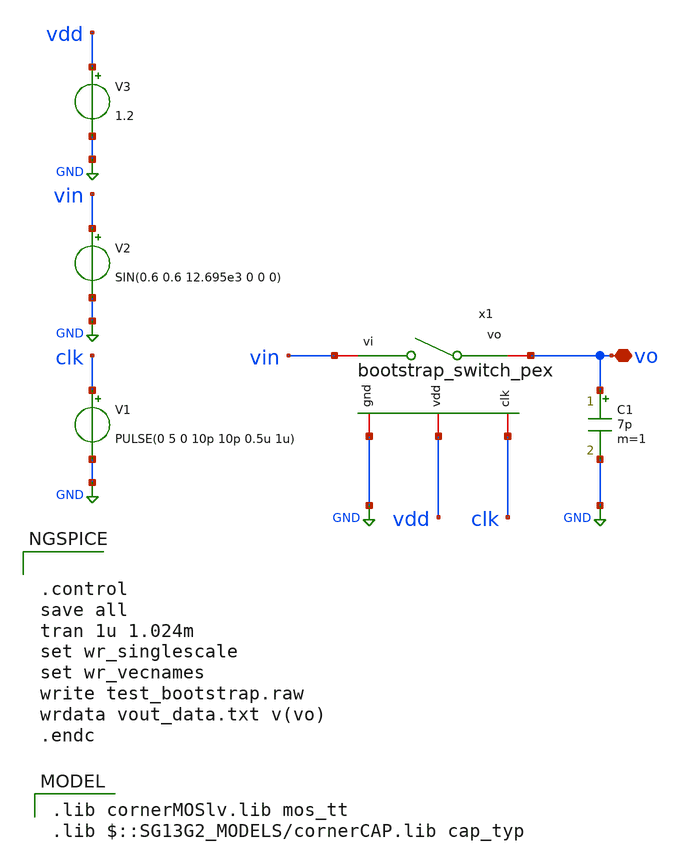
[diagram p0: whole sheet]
** sch_path: dependencies/ADC/ADC-main/schematic/xschem/boostrap_switch_tb_ps.sch
**.subckt boostrap_switch_tb_ps vo
*.iopin vo
V1 clk GND PULSE(0 5 0 10p 10p 0.5u 1u)
V2 vin GND SIN(0.6 0.6 12.695e3 0 0 0)
V3 vdd GND 1.2
C1 vo GND 7p m=1
x1 vdd vin vo clk GND bootstrap_switch_pex
**** begin user architecture code
 .lib cornerMOSlv.lib mos_tt
.lib $::SG13G2_MODELS/cornerCAP.lib cap_typ



.control
save all
tran 1u 1.024m
set wr_singlescale
set wr_vecnames
write test_bootstrap.raw
wrdata vout_data.txt v(vo)
.endc


**** end user architecture code
**.ends

* expanding   symbol:  /home/tien/SAR_ADC_8BIT_IHP/xschem/xschem_pex_symbol/bootstrap_switch_pex.sym
*+ # of pins=5
** sym_path: dependencies/ADC/ADC-main/netlist/pex/xschem_pex_symbol/bootstrap_switch.sym

.subckt bootstrap_switch_pex vdd vi vo clk gnd
X0 gnd.t12 a_1896_n484# a_1378_n288.t0 gnd.t11 sg13_lv_nmos ad=0.136p pd=1.48u as=0.136p ps=1.48u
+ w=0.4u l=0.13u
X1 vi.t0 a_777_n1200.t2 vo.t0 gnd.t4 sg13_lv_nmos ad=0.85p pd=5.68u as=0.85p ps=5.68u w=2.5u l=0.13u
X2 gnd.t15 a_1594_n1108.t3 a_2897_n1624.t0 gnd.t14 sg13_lv_nmos ad=0.136p pd=1.48u as=0.136p
+ ps=1.48u w=0.4u l=0.13u
X3 a_1044_n1116.t0 a_1896_n484# vdd.t6 vdd.t4 sg13_lv_pmos ad=0.17p pd=1.68u as=0.17p ps=1.68u
+ w=0.5u l=0.13u
X4 vdd.t3 clk.t0 a_1594_n1108.t2 vdd.t1 sg13_lv_pmos ad=0.272p pd=2.28u as=0.272p ps=2.28u w=0.8u
+ l=0.13u
X5 vdd.t8 a_2905_n460.t1 w_1241_n212.t2 gnd.t17 sg13_lv_nmos ad=0.442p pd=3.28u as=0.442p ps=3.28u
+ w=1.3u l=0.13u
X6 w_1241_n212.t3 a_1107_n1758.t0 cap_cmim l=6.99u w=9.39u
X7 a_2217_n1270.t0 a_1594_n1108.t4 gnd.t3 gnd.t2 sg13_lv_nmos ad=0.17p pd=1.68u as=0.17p ps=1.68u
+ w=0.5u l=0.13u
X8 a_777_n1200.t0 vdd.t9 a_2217_n1270.t1 gnd.t6 sg13_lv_nmos ad=0.17p pd=1.68u as=0.17p ps=1.68u
+ w=0.5u l=0.13u
X9 gnd.t8 clk.t0 a_1594_n1108.t1 gnd.t7 sg13_lv_nmos ad=0.136p pd=1.48u as=0.136p ps=1.48u w=0.4u
+ l=0.13u
X10 vdd.t5 a_1896_n484# a_1378_n288.t1 vdd.t4 sg13_lv_pmos ad=0.272p pd=2.28u as=0.272p ps=2.28u
+ w=0.8u l=0.13u
X11 vdd.t2 a_1594_n1108.t3 a_2897_n1624.t1 vdd.t1 sg13_lv_pmos ad=0.272p pd=2.28u as=0.272p ps=2.28u
+ w=0.8u l=0.13u
X12 a_2905_n460.t2 a_1594_n1108.t0 cap_cmim l=6.99u w=4.665u
X13 gnd.t1 a_1594_n1108.t5 a_1426_n1756.t0 gnd.t0 sg13_lv_nmos ad=1.02p pd=6.68u as=1.02p ps=6.68u
+ w=3u l=0.13u
X14 a_1107_n1758.t2 a_1044_n1116.t2 vi.t1 gnd.t16 sg13_lv_nmos ad=1.02p pd=6.68u as=1.02p ps=6.68u
+ w=3u l=0.13u
X15 a_3245_n350.t1 a_2897_n1624.t2 cap_cmim l=6.99u w=4.665u
X16 w_1241_n212.t1 a_1378_n288.t2 a_777_n1200.t1 w_1241_n212.t0 sg13_lv_pmos ad=0.17p pd=1.68u
+ as=0.17p ps=1.68u w=0.5u l=0.13u
X17 a_1107_n1758.t1 a_1594_n1108.t6 gnd.t10 gnd.t9 sg13_lv_nmos ad=0.442p pd=3.28u as=0.442p
+ ps=3.28u w=1.3u l=0.4u
X18 a_3245_n350.t0 a_2905_n460.t3 vdd.t0 gnd.t5 sg13_lv_nmos ad=0.442p pd=3.28u as=0.442p ps=3.28u
+ w=1.3u l=0.13u
X19 vdd.t7 a_3245_n350.t2 a_2905_n460.t0 gnd.t13 sg13_lv_nmos ad=0.442p pd=3.28u as=0.442p ps=3.28u
+ w=1.3u l=0.13u
X20 a_1426_n1756.t1 vdd.t10 a_1044_n1116.t1 gnd.t0 sg13_lv_nmos ad=1.02p pd=6.68u as=1.02p ps=6.68u
+ w=3u l=0.13u
C0 a_1896_n484# vdd 0.22188f
C1 vdd vi 0.08373f
C2 vdd clk 0.16174f
C3 vo vi 0.61887f
C4 vo vdd 0.04889f
R0 a_1378_n288.t0 a_1378_n288.n0 17.2852
R1 a_1378_n288.n0 a_1378_n288.t2 16.1733
R2 a_1378_n288.n0 a_1378_n288.t1 9.11151
R3 gnd.n47 gnd.t11 6064.32
R4 gnd.t6 gnd.n18 5073.33
R5 gnd.n58 gnd.n57 4035.37
R6 gnd.n46 gnd.n45 2743.13
R7 gnd.n47 gnd.n46 2249.79
R8 gnd.n45 gnd.t6 1906.67
R9 gnd.n58 gnd.n18 1486.67
R10 gnd.n52 gnd.n51 1186.91
R11 gnd.n55 gnd.n54 447.637
R12 gnd.n63 gnd.n62 302.812
R13 gnd.n59 gnd.n58 181.311
R14 gnd.n63 gnd.t11 123.954
R15 gnd.n52 gnd.t7 82.2655
R16 gnd.n55 gnd.t14 82.2655
R17 gnd.n48 gnd.n47 68.6012
R18 gnd.t17 gnd.n48 65.5295
R19 gnd.n50 gnd.t5 64.9886
R20 gnd.t9 gnd.n59 57.7882
R21 gnd.t13 gnd.n50 49.6349
R22 gnd.t2 gnd.n61 49.0963
R23 gnd.n62 gnd.t2 47.2961
R24 gnd.t16 gnd.t4 40.5082
R25 gnd.n61 gnd.t0 38.6369
R26 gnd.n51 gnd.t13 35.3194
R27 gnd.n60 gnd.t9 31.9293
R28 gnd.n5 gnd.t3 30.9467
R29 gnd.t5 gnd.n49 20.985
R30 gnd.n22 gnd.t8 17.4482
R31 gnd.n64 gnd.t12 17.3778
R32 gnd.n20 gnd.t15 17.3608
R33 gnd.n53 gnd.n52 17.0005
R34 gnd.n56 gnd.n21 17.0005
R35 gnd.n56 gnd.n55 17.0005
R36 gnd.n33 gnd.n19 12.7958
R37 gnd.t4 gnd.n60 12.4856
R38 gnd.n49 gnd.t17 11.7634
R39 gnd.n54 gnd.t7 11.7395
R40 gnd.n57 gnd.t14 11.7395
R41 gnd.n64 gnd.n63 11.3338
R42 gnd.n8 gnd.n7 9.03042
R43 gnd.n74 gnd.n73 9.03042
R44 gnd.n36 gnd.n35 9.03042
R45 gnd.n40 gnd.n39 9.03042
R46 gnd.n72 gnd.n71 9.01861
R47 gnd.n7 gnd.n6 9.0186
R48 gnd.n35 gnd.n34 9.0186
R49 gnd.n27 gnd.n23 9.01787
R50 gnd.n4 gnd.n1 9.01787
R51 gnd.n68 gnd.n10 9.01787
R52 gnd.n32 gnd.n29 9.01787
R53 gnd.n28 gnd.n27 9.01787
R54 gnd.n5 gnd.n4 9.0005
R55 gnd.n3 gnd.n2 9.0005
R56 gnd.n12 gnd.n11 9.0005
R57 gnd.n73 gnd.n72 9.0005
R58 gnd.n13 gnd.n12 9.0005
R59 gnd.n69 gnd.n68 9.0005
R60 gnd.n70 gnd.n69 9.0005
R61 gnd.n31 gnd.n30 9.0005
R62 gnd.n33 gnd.n32 9.0005
R63 gnd.n43 gnd.n42 9.0005
R64 gnd.n25 gnd.n24 9.0005
R65 gnd.n42 gnd.n41 9.0005
R66 gnd.n26 gnd.n25 9.0005
R67 gnd.n41 gnd.n40 9.0005
R68 gnd.n56 gnd.n19 8.52716
R69 gnd.n45 gnd.n17 8.501
R70 gnd.n18 gnd.n16 8.5005
R71 gnd.n48 gnd.n44 8.5005
R72 gnd.n14 gnd.t10 5.65073
R73 gnd.n53 gnd.n22 5.63152
R74 gnd.n43 gnd.n23 4.5471
R75 gnd.n71 gnd.n70 4.54536
R76 gnd.n6 gnd.n5 4.53473
R77 gnd.n34 gnd.n33 4.53473
R78 gnd.n8 gnd.n1 4.50628
R79 gnd.n74 gnd.n10 4.50628
R80 gnd.n36 gnd.n29 4.50628
R81 gnd.n39 gnd.n28 4.50628
R82 gnd.n9 gnd.n8 3.3005
R83 gnd.n39 gnd.n38 3.3005
R84 gnd.n37 gnd.n36 3.3005
R85 gnd.n75 gnd.n74 3.3005
R86 gnd.n44 gnd.n43 2.86049
R87 gnd.n60 gnd.n16 2.66376
R88 gnd.n65 gnd.n17 2.64957
R89 gnd.n57 gnd.n56 2.63175
R90 gnd.n54 gnd.n53 2.63175
R91 gnd.n14 gnd.t1 2.28269
R92 gnd.n70 gnd.n67 2.02138
R93 gnd.t0 gnd.t16 1.62081
R94 gnd.n67 gnd.n66 1.15699
R95 gnd.n67 gnd.n15 0.961754
R96 gnd.n66 gnd.n65 0.859819
R97 gnd.n15 gnd.n14 0.745431
R98 gnd.n22 gnd.n21 0.712801
R99 gnd.n38 gnd.n37 0.52124
R100 gnd.n61 gnd.n16 0.515338
R101 gnd.n16 gnd.n15 0.431601
R102 gnd gnd.n0 0.270611
R103 gnd.n66 gnd.n16 0.199062
R104 gnd.n65 gnd.n64 0.176594
R105 gnd gnd.n76 0.168643
R106 gnd.n76 gnd.n75 0.108906
R107 gnd.n38 gnd.n0 0.0950175
R108 gnd.n20 gnd.n19 0.0773493
R109 gnd gnd.n0 0.0583436
R110 gnd.n75 gnd.n9 0.045325
R111 gnd.n21 gnd.n20 0.0396781
R112 gnd.n7 gnd.n2 0.0357
R113 gnd.n73 gnd.n11 0.0357
R114 gnd.n72 gnd.n12 0.0357
R115 gnd.n35 gnd.n30 0.0357
R116 gnd.n42 gnd.n24 0.0357
R117 gnd.n41 gnd.n25 0.0357
R118 gnd.n40 gnd.n26 0.0357
R119 gnd.n4 gnd.n3 0.0342333
R120 gnd.n68 gnd.n12 0.0342333
R121 gnd.n69 gnd.n13 0.0342333
R122 gnd.n32 gnd.n31 0.0342333
R123 gnd.n27 gnd.n25 0.0342333
R124 gnd.n76 gnd 0.0319332
R125 gnd.n37 gnd.n9 0.0237925
R126 gnd.n6 gnd.n3 0.0185314
R127 gnd.n34 gnd.n31 0.0185314
R128 gnd.n71 gnd.n13 0.0185229
R129 gnd.n2 gnd.n1 0.0178037
R130 gnd.n11 gnd.n10 0.0178037
R131 gnd.n30 gnd.n29 0.0178037
R132 gnd.n28 gnd.n26 0.0178037
R133 gnd.n24 gnd.n23 0.0177958
R134 gnd.n50 gnd.n44 0.00944882
R135 gnd.n62 gnd.n16 0.00513002
R136 gnd.n59 gnd.n16 0.00247443
R137 gnd.n49 gnd.n44 0.00215079
R138 gnd.n51 gnd.n44 0.00129651
R139 gnd.n17 gnd.n16 0.00124999
R140 gnd.n46 gnd.n44 0.00100002
R141 a_777_n1200.t0 a_777_n1200.n0 30.6412
R142 a_777_n1200.n0 a_777_n1200.t1 28.4911
R143 a_777_n1200.n0 a_777_n1200.t2 24.8453
R144 vo vo.t0 8.55687
R145 vi vi.n2 8.03514
R146 vi.n1 vi.t0 5.67075
R147 vi.n1 vi.t1 5.66684
R148 vi.t0 vi.n0 4.24477
R149 vi.t1 vi.n0 3.42449
R150 vi.n2 vi.n1 0.059708
R151 vi.n2 vi.n0 0.042166
R152 a_1594_n1108.n11 a_1594_n1108.n10 32.6771
R153 a_1594_n1108.n7 a_1594_n1108.t1 17.2852
R154 a_1594_n1108.n9 a_1594_n1108.t4 15.8888
R155 a_1594_n1108.n9 a_1594_n1108.t6 15.8447
R156 a_1594_n1108.n8 a_1594_n1108.t3 15.4458
R157 a_1594_n1108.n10 a_1594_n1108.t5 15.0018
R158 a_1594_n1108.n19 a_1594_n1108.n11 10.3793
R159 a_1594_n1108.n11 a_1594_n1108.n8 10.3449
R160 a_1594_n1108.n7 a_1594_n1108.t2 9.11151
R161 a_1594_n1108.n18 a_1594_n1108.n12 9.0005
R162 a_1594_n1108.n19 a_1594_n1108.n18 9.0005
R163 a_1594_n1108.n4 a_1594_n1108.n3 9.0005
R164 a_1594_n1108.n22 a_1594_n1108.n21 9.0005
R165 a_1594_n1108.n14 a_1594_n1108.n6 4.52049
R166 a_1594_n1108.n13 a_1594_n1108.n5 4.51458
R167 a_1594_n1108.n23 a_1594_n1108.n1 4.50536
R168 a_1594_n1108.n14 a_1594_n1108.n2 4.5005
R169 a_1594_n1108.n25 a_1594_n1108.n24 4.5005
R170 a_1594_n1108.n17 a_1594_n1108.n1 4.49517
R171 a_1594_n1108.n26 a_1594_n1108.n0 4.49343
R172 a_1594_n1108.n16 a_1594_n1108.n15 4.49343
R173 a_1594_n1108.n20 a_1594_n1108.n19 4.4932
R174 a_1594_n1108.n15 a_1594_n1108.n13 4.49154
R175 a_1594_n1108.n19 a_1594_n1108.n6 4.49125
R176 a_1594_n1108.n18 a_1594_n1108.n17 3.0005
R177 a_1594_n1108.n24 a_1594_n1108.n2 3.0005
R178 a_1594_n1108.t0 a_1594_n1108.n27 0.777833
R179 a_1594_n1108.n10 a_1594_n1108.n9 0.59856
R180 a_1594_n1108.n8 a_1594_n1108.n7 0.570828
R181 a_1594_n1108.n27 a_1594_n1108.n26 0.106207
R182 a_1594_n1108.n13 a_1594_n1108.n6 0.0402971
R183 a_1594_n1108.n25 a_1594_n1108.n1 0.0239239
R184 a_1594_n1108.n20 a_1594_n1108.n2 0.0166005
R185 a_1594_n1108.n21 a_1594_n1108.n20 0.0166005
R186 a_1594_n1108.n23 a_1594_n1108.n22 0.0166005
R187 a_1594_n1108.n24 a_1594_n1108.n23 0.0166005
R188 a_1594_n1108.n3 a_1594_n1108.n0 0.0161469
R189 a_1594_n1108.n17 a_1594_n1108.n0 0.0161469
R190 a_1594_n1108.n16 a_1594_n1108.n4 0.0161469
R191 a_1594_n1108.n18 a_1594_n1108.n16 0.0161469
R192 a_1594_n1108.t0 a_1594_n1108.n27 0.0129943
R193 a_1594_n1108.n12 a_1594_n1108.n5 0.0126912
R194 a_1594_n1108.n19 a_1594_n1108.n5 0.0126912
R195 a_1594_n1108.n14 a_1594_n1108.n12 0.0118028
R196 a_1594_n1108.n15 a_1594_n1108.n14 0.0115336
R197 a_1594_n1108.n26 a_1594_n1108.n25 0.0115
R198 a_1594_n1108.n21 a_1594_n1108.n4 0.000803448
R199 a_1594_n1108.n22 a_1594_n1108.n3 0.000803448
R200 a_2897_n1624.n22 a_2897_n1624.n21 31.0822
R201 a_2897_n1624.t0 a_2897_n1624.n22 17.2852
R202 a_2897_n1624.n22 a_2897_n1624.t1 9.11151
R203 a_2897_n1624.n11 a_2897_n1624.n8 9.0005
R204 a_2897_n1624.n5 a_2897_n1624.n3 9.0005
R205 a_2897_n1624.n11 a_2897_n1624.n10 9.0005
R206 a_2897_n1624.n9 a_2897_n1624.n3 9.0005
R207 a_2897_n1624.n19 a_2897_n1624.n2 4.50722
R208 a_2897_n1624.n15 a_2897_n1624.n14 4.50536
R209 a_2897_n1624.n16 a_2897_n1624.n4 4.5005
R210 a_2897_n1624.n19 a_2897_n1624.n18 4.5005
R211 a_2897_n1624.n14 a_2897_n1624.n13 4.49517
R212 a_2897_n1624.n20 a_2897_n1624.n1 4.4937
R213 a_2897_n1624.n7 a_2897_n1624.n6 4.49343
R214 a_2897_n1624.n21 a_2897_n1624.n0 4.4932
R215 a_2897_n1624.n13 a_2897_n1624.n12 3.0005
R216 a_2897_n1624.n17 a_2897_n1624.n16 3.0005
R217 a_2897_n1624.n12 a_2897_n1624.n1 3.0005
R218 a_2897_n1624.n18 a_2897_n1624.n17 3.0005
R219 a_2897_n1624.n6 a_2897_n1624.t2 0.119227
R220 a_2897_n1624.n17 a_2897_n1624.n3 0.0317552
R221 a_2897_n1624.n12 a_2897_n1624.n11 0.0308448
R222 a_2897_n1624.n20 a_2897_n1624.n19 0.0297377
R223 a_2897_n1624.n14 a_2897_n1624.n4 0.0239239
R224 a_2897_n1624.n15 a_2897_n1624.n5 0.0166005
R225 a_2897_n1624.n16 a_2897_n1624.n15 0.0166005
R226 a_2897_n1624.n18 a_2897_n1624.n0 0.0166005
R227 a_2897_n1624.n9 a_2897_n1624.n0 0.0166005
R228 a_2897_n1624.n10 a_2897_n1624.n2 0.0161469
R229 a_2897_n1624.n2 a_2897_n1624.n1 0.0161469
R230 a_2897_n1624.n8 a_2897_n1624.n7 0.0161469
R231 a_2897_n1624.n13 a_2897_n1624.n7 0.0161469
R232 a_2897_n1624.n21 a_2897_n1624.n20 0.0156093
R233 a_2897_n1624.n6 a_2897_n1624.n4 0.0115
R234 a_2897_n1624.n8 a_2897_n1624.n5 0.000803448
R235 a_2897_n1624.n11 a_2897_n1624.n3 0.000803448
R236 a_2897_n1624.n10 a_2897_n1624.n9 0.000803448
R237 vdd.n22 vdd.t10 37.129
R238 vdd.n21 vdd.t7 21.2951
R239 vdd.n6 vdd.t6 17.5186
R240 vdd.n2 vdd.n0 17.0005
R241 vdd.t0 vdd.n15 17.0005
R242 vdd.n17 vdd.t0 17.0005
R243 vdd.n16 vdd.t0 17.0005
R244 vdd.t8 vdd.n15 17.0005
R245 vdd.n17 vdd.t8 17.0005
R246 vdd.t8 vdd.n16 17.0005
R247 vdd.n5 vdd.t9 15.4454
R248 vdd.n13 vdd.n12 15.1399
R249 vdd.n20 vdd.n19 12.5536
R250 vdd.n1 vdd.t1 11.2968
R251 vdd.n1 vdd.t3 9.01184
R252 vdd.n19 vdd.n18 9.0005
R253 vdd.n3 vdd.t2 8.91901
R254 vdd.n9 vdd.t5 8.91901
R255 vdd.n10 vdd.n9 8.60851
R256 vdd.n12 vdd.n11 8.501
R257 vdd.n4 vdd.n0 8.46974
R258 vdd.n8 vdd.n7 8.46936
R259 vdd.n11 vdd.t4 5.66842
R260 vdd.t4 vdd.n10 5.66778
R261 vdd.t1 vdd.n0 5.66717
R262 vdd.n19 vdd.n14 4.648
R263 vdd.n6 vdd.n5 3.95314
R264 vdd.n22 vdd.n21 0.908402
R265 vdd.n2 vdd.n1 0.717193
R266 vdd.n5 vdd.n4 0.370276
R267 vdd vdd.n22 0.23247
R268 vdd vdd.n13 0.168921
R269 vdd.n8 vdd.n6 0.164989
R270 vdd.n4 vdd.n3 0.139431
R271 vdd.n9 vdd.n8 0.116961
R272 vdd.n3 vdd.n2 0.0531761
R273 vdd.n20 vdd.n13 0.0498354
R274 vdd.n18 vdd.n17 0.0452964
R275 vdd.n21 vdd.n20 0.0287622
R276 vdd.n16 vdd.n14 0.0274732
R277 vdd.n17 vdd.n14 0.024195
R278 vdd.n18 vdd.n15 0.00547738
R279 vdd.n12 vdd.n6 0.00173596
R280 vdd.n10 vdd.n7 0.00166667
R281 vdd.n11 vdd.n7 0.00124999
R282 a_1044_n1116.t0 a_1044_n1116.n0 57.304
R283 a_1044_n1116.n0 a_1044_n1116.t2 15.0005
R284 a_1044_n1116.n0 a_1044_n1116.t1 3.77826
R285 clk clk.t0 39.2421
R286 a_2905_n460.n20 a_2905_n460.n19 21.2719
R287 a_2905_n460.n20 a_2905_n460.t1 15.858
R288 a_2905_n460.n21 a_2905_n460.t3 15.0005
R289 a_2905_n460.n13 a_2905_n460.n12 9.0005
R290 a_2905_n460.n13 a_2905_n460.n7 9.0005
R291 a_2905_n460.n15 a_2905_n460.n14 9.0005
R292 a_2905_n460.n5 a_2905_n460.n3 9.0005
R293 a_2905_n460.n6 a_2905_n460.n5 9.0005
R294 a_2905_n460.t0 a_2905_n460.n21 6.95387
R295 a_2905_n460.n18 a_2905_n460.n2 4.52049
R296 a_2905_n460.n18 a_2905_n460.n17 4.5005
R297 a_2905_n460.n9 a_2905_n460.n8 4.49515
R298 a_2905_n460.n19 a_2905_n460.n0 4.49343
R299 a_2905_n460.n16 a_2905_n460.n6 4.4932
R300 a_2905_n460.n19 a_2905_n460.n1 4.49154
R301 a_2905_n460.n6 a_2905_n460.n2 4.49125
R302 a_2905_n460.n11 a_2905_n460.n10 3.03054
R303 a_2905_n460.n17 a_2905_n460.n4 3.00885
R304 a_2905_n460.n10 a_2905_n460.n9 3.0005
R305 a_2905_n460.n12 a_2905_n460.n4 2.26296
R306 a_2905_n460.n11 a_2905_n460.t2 2.24339
R307 a_2905_n460.n2 a_2905_n460.n1 0.0402971
R308 a_2905_n460.n13 a_2905_n460.n10 0.0308448
R309 a_2905_n460.n14 a_2905_n460.n4 0.0243199
R310 a_2905_n460.n5 a_2905_n460.n1 0.0199256
R311 a_2905_n460.n16 a_2905_n460.n15 0.0166005
R312 a_2905_n460.n17 a_2905_n460.n16 0.0166005
R313 a_2905_n460.n7 a_2905_n460.n0 0.0161469
R314 a_2905_n460.n9 a_2905_n460.n0 0.0161469
R315 a_2905_n460.n8 a_2905_n460.n6 0.0126912
R316 a_2905_n460.n8 a_2905_n460.n3 0.0126912
R317 a_2905_n460.n18 a_2905_n460.n3 0.0118028
R318 a_2905_n460.n19 a_2905_n460.n18 0.0115336
R319 a_2905_n460.n21 a_2905_n460.n20 0.00521429
R320 a_2905_n460.n12 a_2905_n460.n11 0.000803448
R321 a_2905_n460.n14 a_2905_n460.n13 0.000803448
R322 a_2905_n460.n15 a_2905_n460.n7 0.000803448
R323 w_1241_n212.t1 w_1241_n212.n16 17.0005
R324 w_1241_n212.n15 w_1241_n212.n14 13.8861
R325 w_1241_n212.n16 w_1241_n212.n15 12.959
R326 w_1241_n212.n16 w_1241_n212.t0 11.815
R327 w_1241_n212.n15 w_1241_n212.t2 9.40506
R328 w_1241_n212.n8 w_1241_n212.n7 9.0005
R329 w_1241_n212.n3 w_1241_n212.n2 9.0005
R330 w_1241_n212.n7 w_1241_n212.n6 9.0005
R331 w_1241_n212.n2 w_1241_n212.n1 9.0005
R332 w_1241_n212.n1 w_1241_n212.n0 9.0005
R333 w_1241_n212.n12 w_1241_n212.n11 3.00885
R334 w_1241_n212.n5 w_1241_n212.n4 3.00864
R335 w_1241_n212.n9 w_1241_n212.n4 3.00862
R336 w_1241_n212.n13 w_1241_n212.n12 3.0005
R337 w_1241_n212.n14 w_1241_n212.n13 3.0005
R338 w_1241_n212.n5 w_1241_n212.n0 2.26694
R339 w_1241_n212.n11 w_1241_n212.n10 2.26266
R340 w_1241_n212.n10 w_1241_n212.n9 2.26263
R341 w_1241_n212.n10 w_1241_n212.t3 2.23387
R342 w_1241_n212.n14 w_1241_n212.n0 0.039569
R343 w_1241_n212.n12 w_1241_n212.n2 0.0317552
R344 w_1241_n212.n13 w_1241_n212.n1 0.0317552
R345 w_1241_n212.n7 w_1241_n212.n4 0.0308448
R346 w_1241_n212.n11 w_1241_n212.n3 0.0243199
R347 w_1241_n212.n9 w_1241_n212.n8 0.0236441
R348 w_1241_n212.n6 w_1241_n212.n5 0.0236299
R349 w_1241_n212.n8 w_1241_n212.n3 0.000803448
R350 w_1241_n212.n7 w_1241_n212.n2 0.000803448
R351 w_1241_n212.n6 w_1241_n212.n1 0.000803448
R352 a_1107_n1758.n15 a_1107_n1758.t1 17.0517
R353 a_1107_n1758.n14 a_1107_n1758.n13 9.14174
R354 a_1107_n1758.n15 a_1107_n1758.n14 9.04245
R355 a_1107_n1758.n12 a_1107_n1758.n4 9.0005
R356 a_1107_n1758.n10 a_1107_n1758.n9 9.0005
R357 a_1107_n1758.n4 a_1107_n1758.n3 9.0005
R358 a_1107_n1758.n9 a_1107_n1758.n8 9.0005
R359 a_1107_n1758.n7 a_1107_n1758.n3 9.0005
R360 a_1107_n1758.n17 a_1107_n1758.n16 8.92852
R361 a_1107_n1758.t1 a_1107_n1758.n13 8.48635
R362 a_1107_n1758.n14 a_1107_n1758.t2 5.34524
R363 a_1107_n1758.n2 a_1107_n1758.n1 4.50536
R364 a_1107_n1758.n21 a_1107_n1758.n20 4.5005
R365 a_1107_n1758.n5 a_1107_n1758.n1 4.49517
R366 a_1107_n1758.n22 a_1107_n1758.n0 4.49343
R367 a_1107_n1758.n11 a_1107_n1758.n6 3.00864
R368 a_1107_n1758.n18 a_1107_n1758.n17 3.0005
R369 a_1107_n1758.n19 a_1107_n1758.n18 3.0005
R370 a_1107_n1758.n6 a_1107_n1758.n5 3.0005
R371 a_1107_n1758.n20 a_1107_n1758.n19 3.0005
R372 a_1107_n1758.n12 a_1107_n1758.n11 2.26694
R373 a_1107_n1758.t0 a_1107_n1758.n23 1.06017
R374 a_1107_n1758.n23 a_1107_n1758.n22 0.104061
R375 a_1107_n1758.n16 a_1107_n1758.n13 0.0718134
R376 a_1107_n1758.n16 a_1107_n1758.n15 0.0529419
R377 a_1107_n1758.n17 a_1107_n1758.n12 0.039569
R378 a_1107_n1758.n18 a_1107_n1758.n4 0.0317552
R379 a_1107_n1758.n19 a_1107_n1758.n3 0.0317552
R380 a_1107_n1758.n9 a_1107_n1758.n6 0.0308448
R381 a_1107_n1758.n21 a_1107_n1758.n1 0.0239239
R382 a_1107_n1758.n11 a_1107_n1758.n10 0.0236299
R383 a_1107_n1758.n7 a_1107_n1758.n2 0.0166005
R384 a_1107_n1758.n20 a_1107_n1758.n2 0.0166005
R385 a_1107_n1758.n5 a_1107_n1758.n0 0.0161469
R386 a_1107_n1758.n8 a_1107_n1758.n0 0.0161469
R387 a_1107_n1758.t0 a_1107_n1758.n23 0.0120563
R388 a_1107_n1758.n22 a_1107_n1758.n21 0.0115
R389 a_1107_n1758.n10 a_1107_n1758.n4 0.000803448
R390 a_1107_n1758.n9 a_1107_n1758.n3 0.000803448
R391 a_1107_n1758.n8 a_1107_n1758.n7 0.000803448
R392 a_2217_n1270.t0 a_2217_n1270.t1 34.1149
R393 a_1426_n1756.t0 a_1426_n1756.t1 4.25425
R394 a_3245_n350.n20 a_3245_n350.n19 22.1589
R395 a_3245_n350.t0 a_3245_n350.n0 17.0005
R396 a_3245_n350.n0 a_3245_n350.t2 16.0463
R397 a_3245_n350.n14 a_3245_n350.n13 9.0005
R398 a_3245_n350.n13 a_3245_n350.n12 9.0005
R399 a_3245_n350.n5 a_3245_n350.n4 9.0005
R400 a_3245_n350.n12 a_3245_n350.n11 9.0005
R401 a_3245_n350.n10 a_3245_n350.n4 9.0005
R402 a_3245_n350.t0 a_3245_n350.n20 8.5689
R403 a_3245_n350.n3 a_3245_n350.n2 4.50831
R404 a_3245_n350.n18 a_3245_n350.n17 4.5005
R405 a_3245_n350.n8 a_3245_n350.n2 4.4937
R406 a_3245_n350.n19 a_3245_n350.n1 4.49343
R407 a_3245_n350.n7 a_3245_n350.n6 3.02902
R408 a_3245_n350.n16 a_3245_n350.n15 3.00885
R409 a_3245_n350.n9 a_3245_n350.n7 3.0005
R410 a_3245_n350.n9 a_3245_n350.n8 3.0005
R411 a_3245_n350.n17 a_3245_n350.n16 3.0005
R412 a_3245_n350.n15 a_3245_n350.n14 2.26296
R413 a_3245_n350.n6 a_3245_n350.t1 2.243
R414 a_3245_n350.n20 a_3245_n350.n0 0.142709
R415 a_3245_n350.n16 a_3245_n350.n4 0.0317552
R416 a_3245_n350.n13 a_3245_n350.n7 0.0308448
R417 a_3245_n350.n12 a_3245_n350.n9 0.0308448
R418 a_3245_n350.n18 a_3245_n350.n2 0.0297377
R419 a_3245_n350.n15 a_3245_n350.n5 0.0243199
R420 a_3245_n350.n17 a_3245_n350.n3 0.0166005
R421 a_3245_n350.n10 a_3245_n350.n3 0.0166005
R422 a_3245_n350.n11 a_3245_n350.n1 0.0161469
R423 a_3245_n350.n8 a_3245_n350.n1 0.0161469
R424 a_3245_n350.n19 a_3245_n350.n18 0.014292
R425 a_3245_n350.n14 a_3245_n350.n6 0.00232069
R426 a_3245_n350.n13 a_3245_n350.n5 0.000803448
R427 a_3245_n350.n12 a_3245_n350.n4 0.000803448
R428 a_3245_n350.n11 a_3245_n350.n10 0.000803448
C5 clk gnd 1.31453f
C6 vo gnd 1.08409f
C7 vi gnd 1.01467f
C8 vdd gnd 17.3224f
C9 a_1896_n484# gnd 0.5027f $ **FLOATING
.ends

.GLOBAL GND
.end
